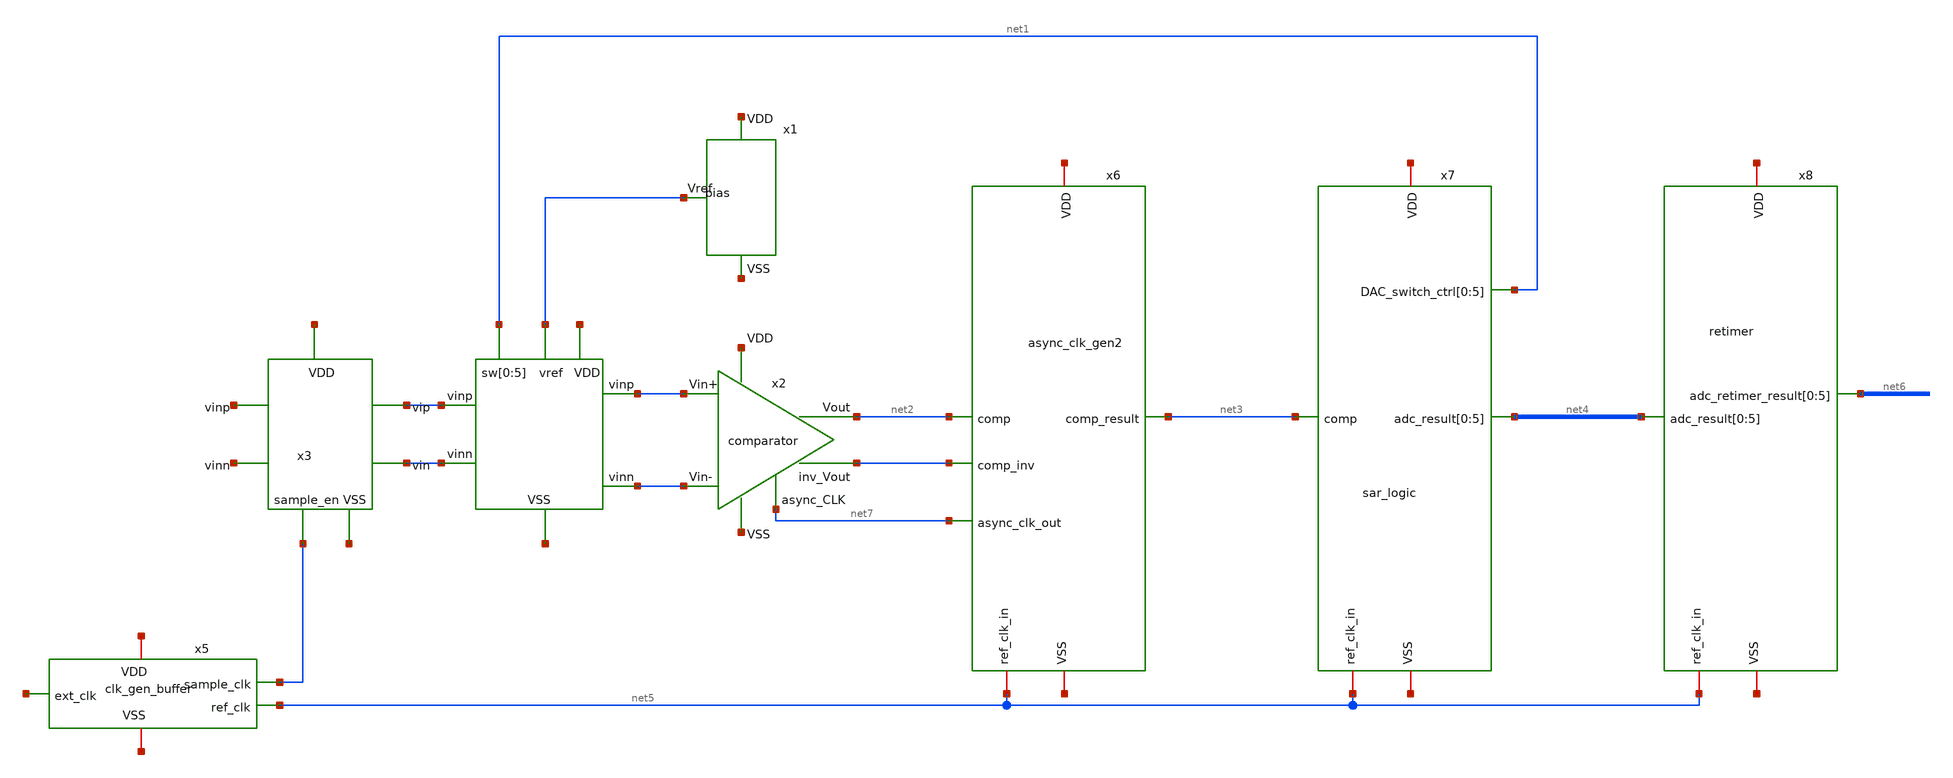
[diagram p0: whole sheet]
** sch_path: just_sym/6bit_SAR_ADC_top.sch
**.subckt 6bit_SAR_ADC_top
x1 net8 net9 net1 bias
x2 net10 net1 net11 net1 net2 net7 comparator
x5 net12 net13 net1 net14 net5 clk_gen_buffer
x6 net15 net16 net2 net2 net3 net7 net5 async_clk_gen2
x7 net17 net18 net3 net4[5] net4[4] net4[3] net4[2] net4[1] net4[0] net5 net1 net1 net1 net1 net1
+ net1 sar_logic
**.ends
.end
